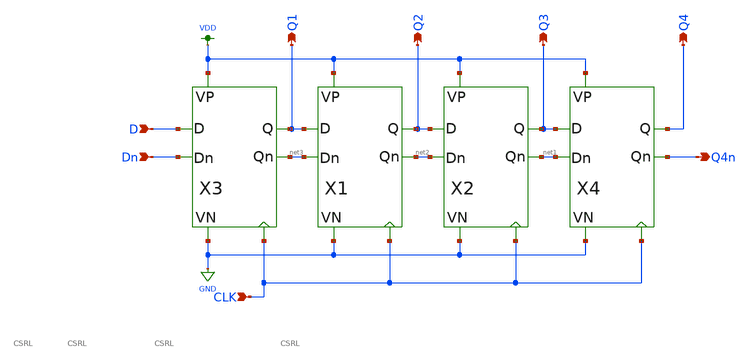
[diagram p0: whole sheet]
** sch_path: shiftreg.sch
**.subckt shiftreg D Dn CLK Q1 Q2 Q3 Q4 Q4n
*.ipin D
*.ipin Dn
*.ipin CLK
*.opin Q1
*.opin Q2
*.opin Q3
*.opin Q4
*.opin Q4n
X3 D Dn VDD GND net3 Q1 CLK CSRL
X1 Q1 net3 VDD GND net2 Q2 CLK CSRL
X2 Q2 net2 VDD GND net1 Q3 CLK CSRL
X4 Q3 net1 VDD GND Q4n Q4 CLK CSRL
**.ends

* expanding   symbol:  /home/jonah/VLSI/MP2/CSRL.sym # of pins=7
** sym_path: CSRL.sym
** sch_path: CSRL.sch
.subckt CSRL D Dn VP VN Qn Q CLK
*.ipin CLK
*.iopin VN
*.iopin VP
*.iopin D
*.iopin Dn
*.iopin Q
*.iopin Qn
XM1 net1 CLK VN GND sky130_fd_pr__nfet_01v8 L=0.15 W=1 nf=1 ad='int((nf+1)/2) * W/nf * 0.29' as='int((nf+2)/2) * W/nf * 0.29'
+ pd='2*int((nf+1)/2) * (W/nf + 0.29)' ps='2*int((nf+2)/2) * (W/nf + 0.29)' nrd='0.29 / W' nrs='0.29 / W'
+ sa=0 sb=0 sd=0 mult=1 m=1
XM2 net1 net2 net3 GND sky130_fd_pr__nfet_01v8 L=0.15 W=1 nf=1 ad='int((nf+1)/2) * W/nf * 0.29' as='int((nf+2)/2) * W/nf * 0.29'
+ pd='2*int((nf+1)/2) * (W/nf + 0.29)' ps='2*int((nf+2)/2) * (W/nf + 0.29)' nrd='0.29 / W' nrs='0.29 / W'
+ sa=0 sb=0 sd=0 mult=1 m=1
XM3 net1 net3 net2 GND sky130_fd_pr__nfet_01v8 L=0.15 W=1 nf=1 ad='int((nf+1)/2) * W/nf * 0.29' as='int((nf+2)/2) * W/nf * 0.29'
+ pd='2*int((nf+1)/2) * (W/nf + 0.29)' ps='2*int((nf+2)/2) * (W/nf + 0.29)' nrd='0.29 / W' nrs='0.29 / W'
+ sa=0 sb=0 sd=0 mult=1 m=1
XM4 Qn CLK net2 GND sky130_fd_pr__nfet_01v8 L=0.15*4 W=1 nf=1 ad='int((nf+1)/2) * W/nf * 0.29' as='int((nf+2)/2) * W/nf * 0.29'
+ pd='2*int((nf+1)/2) * (W/nf + 0.29)' ps='2*int((nf+2)/2) * (W/nf + 0.29)' nrd='0.29 / W' nrs='0.29 / W'
+ sa=0 sb=0 sd=0 mult=1 m=1
XM5 Q CLK net3 GND sky130_fd_pr__nfet_01v8 L=0.15*4 W=1 nf=1 ad='int((nf+1)/2) * W/nf * 0.29' as='int((nf+2)/2) * W/nf * 0.29'
+ pd='2*int((nf+1)/2) * (W/nf + 0.29)' ps='2*int((nf+2)/2) * (W/nf + 0.29)' nrd='0.29 / W' nrs='0.29 / W'
+ sa=0 sb=0 sd=0 mult=1 m=1
XM6 VN Q Qn GND sky130_fd_pr__nfet_01v8 L=0.15 W=1 nf=1 ad='int((nf+1)/2) * W/nf * 0.29' as='int((nf+2)/2) * W/nf * 0.29'
+ pd='2*int((nf+1)/2) * (W/nf + 0.29)' ps='2*int((nf+2)/2) * (W/nf + 0.29)' nrd='0.29 / W' nrs='0.29 / W'
+ sa=0 sb=0 sd=0 mult=1 m=1
XM7 VN Qn Q GND sky130_fd_pr__nfet_01v8 L=0.15 W=1 nf=1 ad='int((nf+1)/2) * W/nf * 0.29' as='int((nf+2)/2) * W/nf * 0.29'
+ pd='2*int((nf+1)/2) * (W/nf + 0.29)' ps='2*int((nf+2)/2) * (W/nf + 0.29)' nrd='0.29 / W' nrs='0.29 / W'
+ sa=0 sb=0 sd=0 mult=1 m=1
XM8 net2 net3 VP VDD sky130_fd_pr__pfet_01v8 L=0.15 W=1 nf=1 ad='int((nf+1)/2) * W/nf * 0.29' as='int((nf+2)/2) * W/nf * 0.29'
+ pd='2*int((nf+1)/2) * (W/nf + 0.29)' ps='2*int((nf+2)/2) * (W/nf + 0.29)' nrd='0.29 / W' nrs='0.29 / W'
+ sa=0 sb=0 sd=0 mult=1 m=1
XM9 net2 CLK Dn VDD sky130_fd_pr__pfet_01v8 L=0.15*4 W=1 nf=1 ad='int((nf+1)/2) * W/nf * 0.29' as='int((nf+2)/2) * W/nf * 0.29'
+ pd='2*int((nf+1)/2) * (W/nf + 0.29)' ps='2*int((nf+2)/2) * (W/nf + 0.29)' nrd='0.29 / W' nrs='0.29 / W'
+ sa=0 sb=0 sd=0 mult=1 m=1
XM10 net3 net2 VP VDD sky130_fd_pr__pfet_01v8 L=0.15 W=1 nf=1 ad='int((nf+1)/2) * W/nf * 0.29' as='int((nf+2)/2) * W/nf * 0.29'
+ pd='2*int((nf+1)/2) * (W/nf + 0.29)' ps='2*int((nf+2)/2) * (W/nf + 0.29)' nrd='0.29 / W' nrs='0.29 / W'
+ sa=0 sb=0 sd=0 mult=1 m=1
XM11 net3 CLK D VDD sky130_fd_pr__pfet_01v8 L=0.15*4 W=1 nf=1 ad='int((nf+1)/2) * W/nf * 0.29' as='int((nf+2)/2) * W/nf * 0.29'
+ pd='2*int((nf+1)/2) * (W/nf + 0.29)' ps='2*int((nf+2)/2) * (W/nf + 0.29)' nrd='0.29 / W' nrs='0.29 / W'
+ sa=0 sb=0 sd=0 mult=1 m=1
XM12 net4 CLK VP VDD sky130_fd_pr__pfet_01v8 L=0.15 W=1 nf=1 ad='int((nf+1)/2) * W/nf * 0.29' as='int((nf+2)/2) * W/nf * 0.29'
+ pd='2*int((nf+1)/2) * (W/nf + 0.29)' ps='2*int((nf+2)/2) * (W/nf + 0.29)' nrd='0.29 / W' nrs='0.29 / W'
+ sa=0 sb=0 sd=0 mult=1 m=1
XM13 Q Qn net4 VDD sky130_fd_pr__pfet_01v8 L=0.15 W=1 nf=1 ad='int((nf+1)/2) * W/nf * 0.29' as='int((nf+2)/2) * W/nf * 0.29'
+ pd='2*int((nf+1)/2) * (W/nf + 0.29)' ps='2*int((nf+2)/2) * (W/nf + 0.29)' nrd='0.29 / W' nrs='0.29 / W'
+ sa=0 sb=0 sd=0 mult=1 m=1
XM14 Qn Q net4 VDD sky130_fd_pr__pfet_01v8 L=0.15 W=1 nf=1 ad='int((nf+1)/2) * W/nf * 0.29' as='int((nf+2)/2) * W/nf * 0.29'
+ pd='2*int((nf+1)/2) * (W/nf + 0.29)' ps='2*int((nf+2)/2) * (W/nf + 0.29)' nrd='0.29 / W' nrs='0.29 / W'
+ sa=0 sb=0 sd=0 mult=1 m=1
.ends

.GLOBAL GND
.GLOBAL VDD
.end
